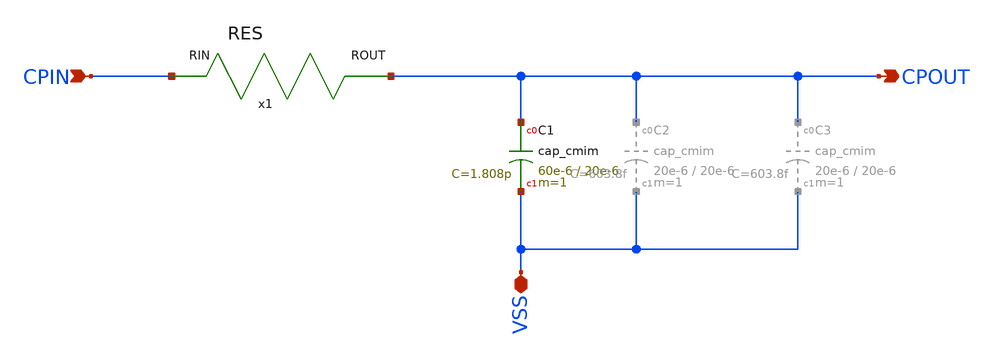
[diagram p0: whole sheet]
** sch_path: QDLL6501-main/schematic/xschem/CP.sch
**.subckt CP VSS CPIN CPOUT
*.iopin VSS
*.ipin CPIN
*.opin CPOUT
XC1 CPOUT VSS cap_cmim w=60e-6 l=20e-6 m=1 mm_ok=1
x1 CPOUT CPIN RES
**.ends

* expanding   symbol:
*+  IHP__MPC0349/dependencies/IHP__QDLL6501/QDLL6501-main/schematic/xschem/RES.sym # of pins=2
** sym_path: QDLL6501-main/schematic/xschem/RES.sym
** sch_path: QDLL6501-main/schematic/xschem/RES.sch
.subckt RES ROUT RIN
*.ipin RIN
*.opin ROUT
XR13 net1 RIN VSS rppd w=1e-6 l=10e-6 m=1 b=0 mm_ok=1
XR1 net2 net1 VSS rppd w=1e-6 l=10e-6 m=1 b=0 mm_ok=1
XR2 net3 net2 VSS rppd w=1e-6 l=10e-6 m=1 b=0 mm_ok=1
XR3 net4 net3 VSS rppd w=1e-6 l=10e-6 m=1 b=0 mm_ok=1
XR4 net5 net4 VSS rppd w=1e-6 l=10e-6 m=1 b=0 mm_ok=1
XR5 net6 net5 VSS rppd w=1e-6 l=10e-6 m=1 b=0 mm_ok=1
XR6 net7 net6 VSS rppd w=1e-6 l=10e-6 m=1 b=0 mm_ok=1
XR7 net8 net7 VSS rppd w=1e-6 l=10e-6 m=1 b=0 mm_ok=1
XR8 net9 net8 VSS rppd w=1e-6 l=10e-6 m=1 b=0 mm_ok=1
XR9 net10 net9 VSS rppd w=1e-6 l=10e-6 m=1 b=0 mm_ok=1
XR10 net11 net10 VSS rppd w=1e-6 l=10e-6 m=1 b=0 mm_ok=1
XR11 ROUT net11 VSS rppd w=1e-6 l=10e-6 m=1 b=0 mm_ok=1
.ends

.end
